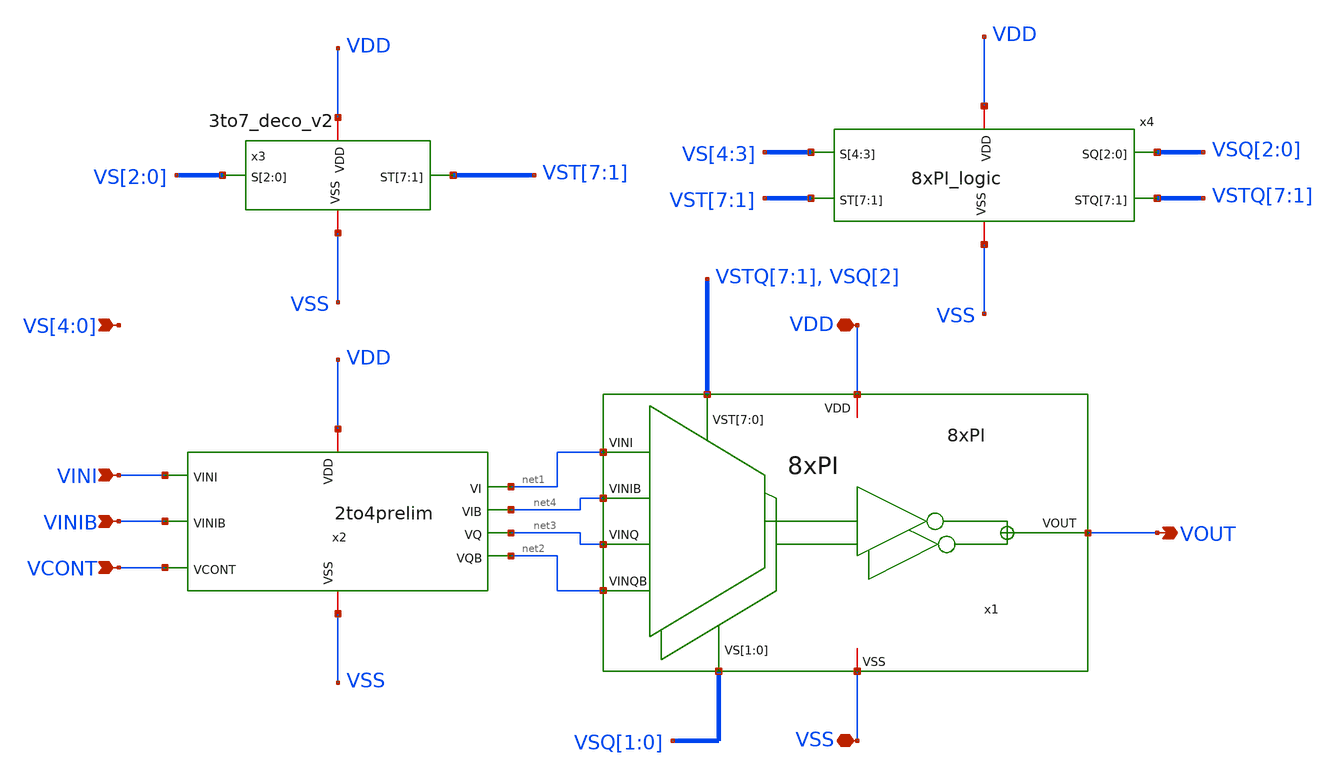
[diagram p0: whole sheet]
** sch_path: 8xPI_top/8xPI_top.sch
**.subckt 8xPI_top VINI VINIB VCONT VDD VSS VOUT VS[4],VS[3],VS[2],VS[1],VS[0]
*.ipin VINI
*.ipin VINIB
*.ipin VCONT
*.iopin VDD
*.iopin VSS
*.opin VOUT
*.ipin VS[4],VS[3],VS[2],VS[1],VS[0]
x1 net1 net4 net3 net2 VSQ[1] VSQ[0] VSTQ[7] VSTQ[6] VSTQ[5] VSTQ[4] VSTQ[3] VSTQ[2] VSTQ[1] VSQ[2]
+ VOUT VDD VSS 8xPI
x2 VDD net2 net3 VINI VSS VCONT net4 net1 VINIB 2to4prelim
x3 VST[7] VST[6] VST[5] VST[4] VST[3] VST[2] VST[1] VS[2] VS[1] VS[0] VDD VSS 3to7_deco_v2
x4 VDD VSQ[2] VSQ[1] VSQ[0] VS[4] VS[3] VSS VSTQ[7] VSTQ[6] VSTQ[5] VSTQ[4] VSTQ[3] VSTQ[2] VSTQ[1]
+ VST[7] VST[6] VST[5] VST[4] VST[3] VST[2] VST[1] 8xPI_logic
**.ends
.end
